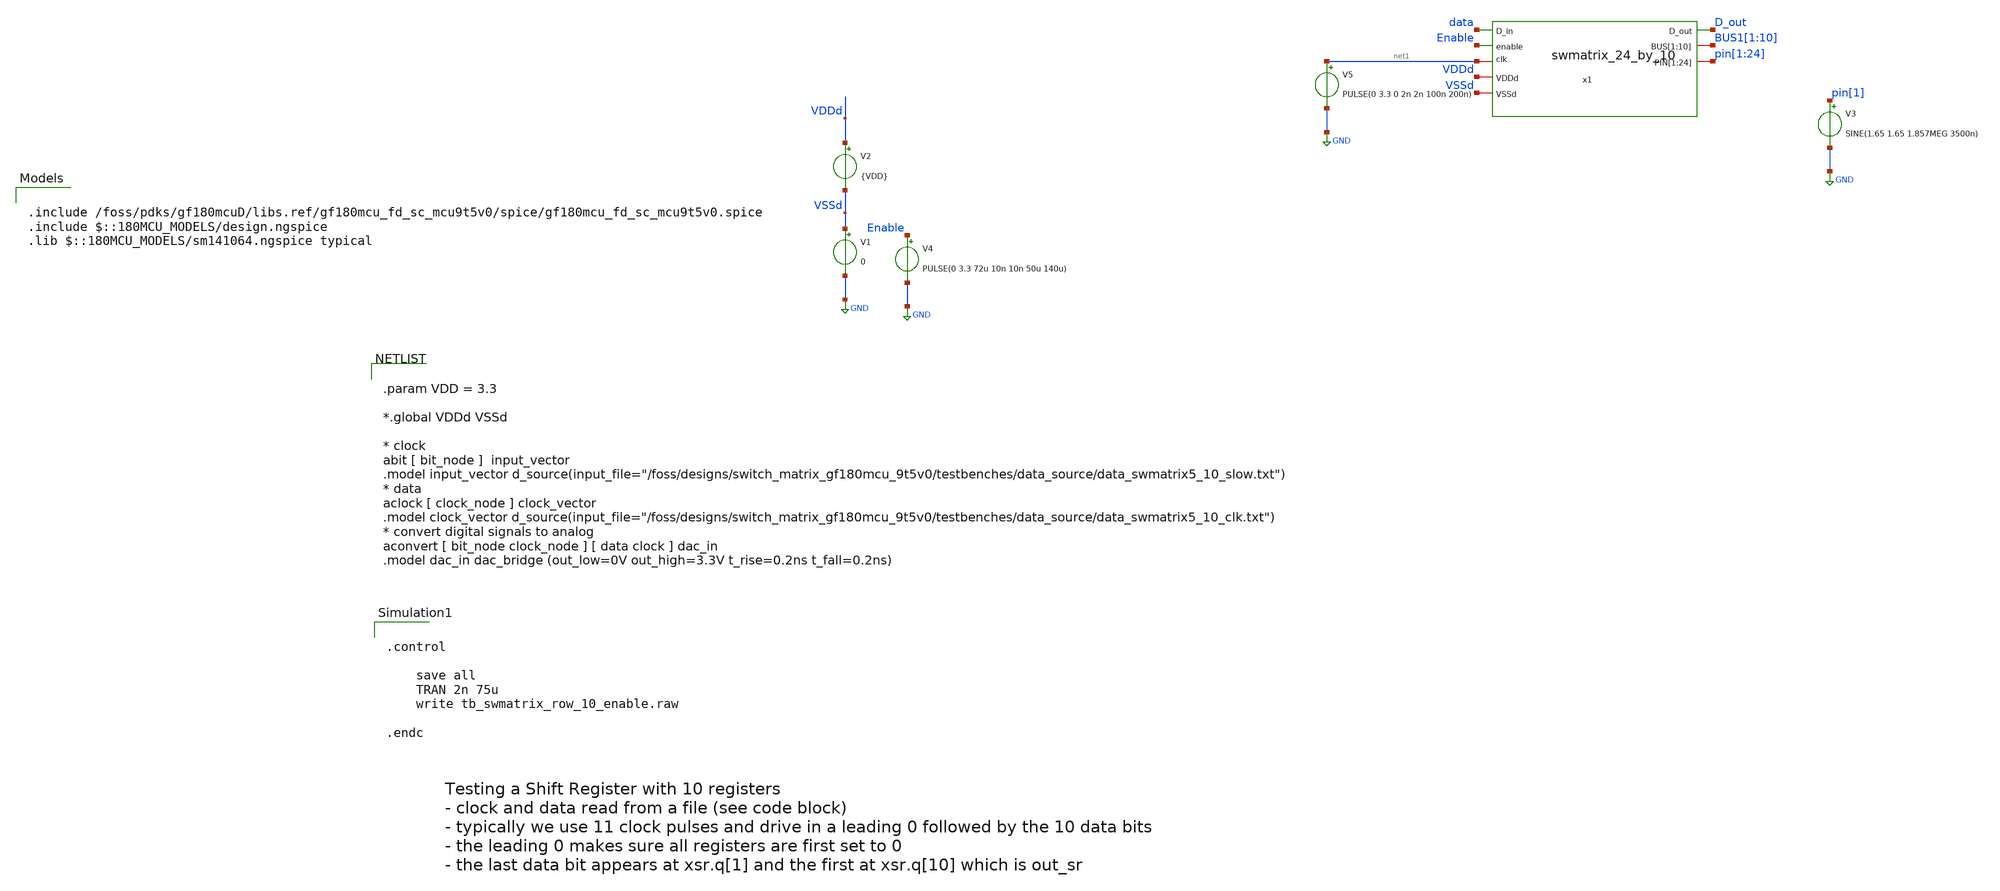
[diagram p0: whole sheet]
** sch_path: testbenches/tb_swmatrix_24_10/tb_swmatrix_24_by_10_slow_clk_dat.sch
**.subckt tb_swmatrix_24_by_10_slow_clk_dat
V1 VSSd GND 0
V2 VDDd VSSd {VDD}
V3 pin[1] GND SINE(1.65 1.65 1.857MEG 3500n)
V4 Enable GND PULSE(0 3.3 72u 10n 10n 50u 140u)
x1 D_out BUS1[1] BUS1[2] BUS1[3] BUS1[4] BUS1[5] BUS1[6] BUS1[7] BUS1[8] BUS1[9] BUS1[10] pin[1]
+ pin[2] pin[3] pin[4] pin[5] pin[6] pin[7] pin[8] pin[9] pin[10] pin[11] pin[12] pin[13] pin[14] pin[15]
+ pin[16] pin[17] pin[18] pin[19] pin[20] pin[21] pin[22] pin[23] pin[24] data VDDd Enable VSSd net1
+ swmatrix_24_by_10
V5 net1 GND PULSE(0 3.3 0 2n 2n 100n 200n)
**** begin user architecture code

.include /foss/pdks/gf180mcuD/libs.ref/gf180mcu_fd_sc_mcu9t5v0/spice/gf180mcu_fd_sc_mcu9t5v0.spice
.include $::180MCU_MODELS/design.ngspice
.lib $::180MCU_MODELS/sm141064.ngspice typical



.param VDD = 3.3

*.global VDDd VSSd

* clock
abit [ bit_node ]  input_vector
.model input_vector
+ d_source(input_file="/foss/designs/switch_matrix_gf180mcu_9t5v0/testbenches/data_source/data_swmatrix5_10_slow.txt")
* data
aclock [ clock_node ] clock_vector
.model clock_vector
+ d_source(input_file="/foss/designs/switch_matrix_gf180mcu_9t5v0/testbenches/data_source/data_swmatrix5_10_clk.txt")
* convert digital signals to analog
aconvert [ bit_node clock_node ] [ data clock ] dac_in
.model dac_in dac_bridge (out_low=0V out_high=3.3V t_rise=0.2ns t_fall=0.2ns)




.control

    save all
    TRAN 2n 75u
    write tb_swmatrix_row_10_enable.raw

.endc


**** end user architecture code
**.ends
.GLOBAL GND
.end
